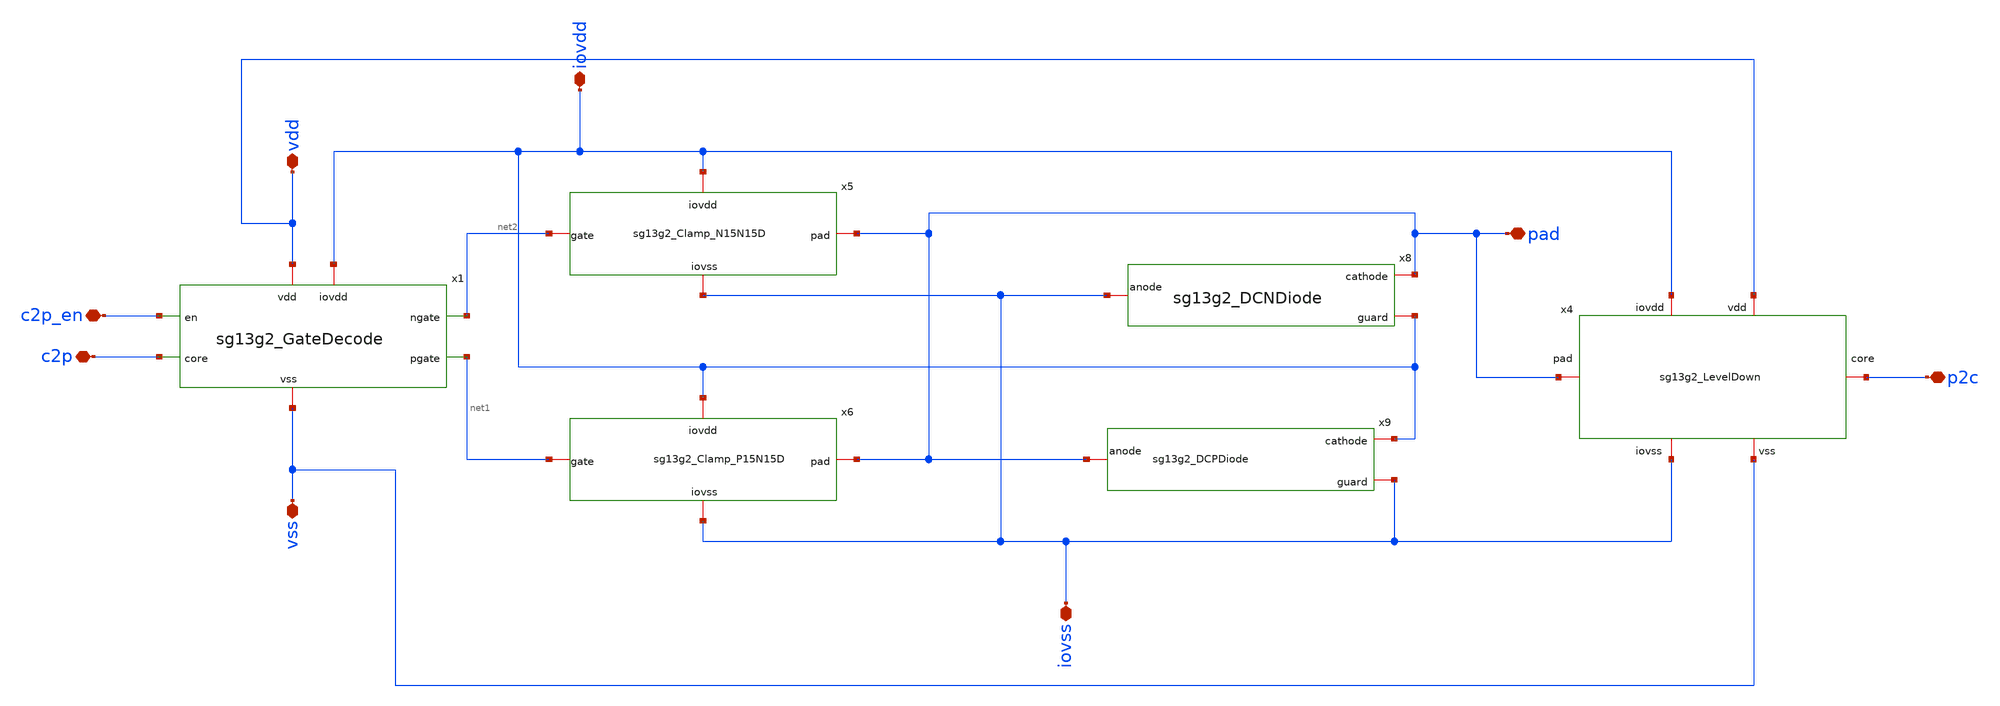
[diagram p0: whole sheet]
** sch_path: CDR4176-main/schematic/xschem/project_io/sg13g2_IOPadInOut30mA/sg13g2_IOPadInOut30mA.sch
**.subckt sg13g2_IOPadInOut30mA iovss pad vss c2p vdd iovdd c2p_en p2c
*.iopin iovss
*.iopin pad
*.iopin vss
*.iopin c2p
*.iopin vdd
*.iopin iovdd
*.iopin c2p_en
*.iopin p2c
x8 pad iovss iovdd sg13g2_DCNDiode
x9 iovdd pad iovss sg13g2_DCPDiode
x1 vdd iovdd c2p_en net2 net1 c2p vss sg13g2_GateDecode
x4 vdd iovdd p2c pad iovss vss sg13g2_LevelDown
x5 iovdd pad net2 iovss sg13g2_Clamp_N15N15D
x6 iovdd net1 pad iovss sg13g2_Clamp_P15N15D
**.ends
.end
